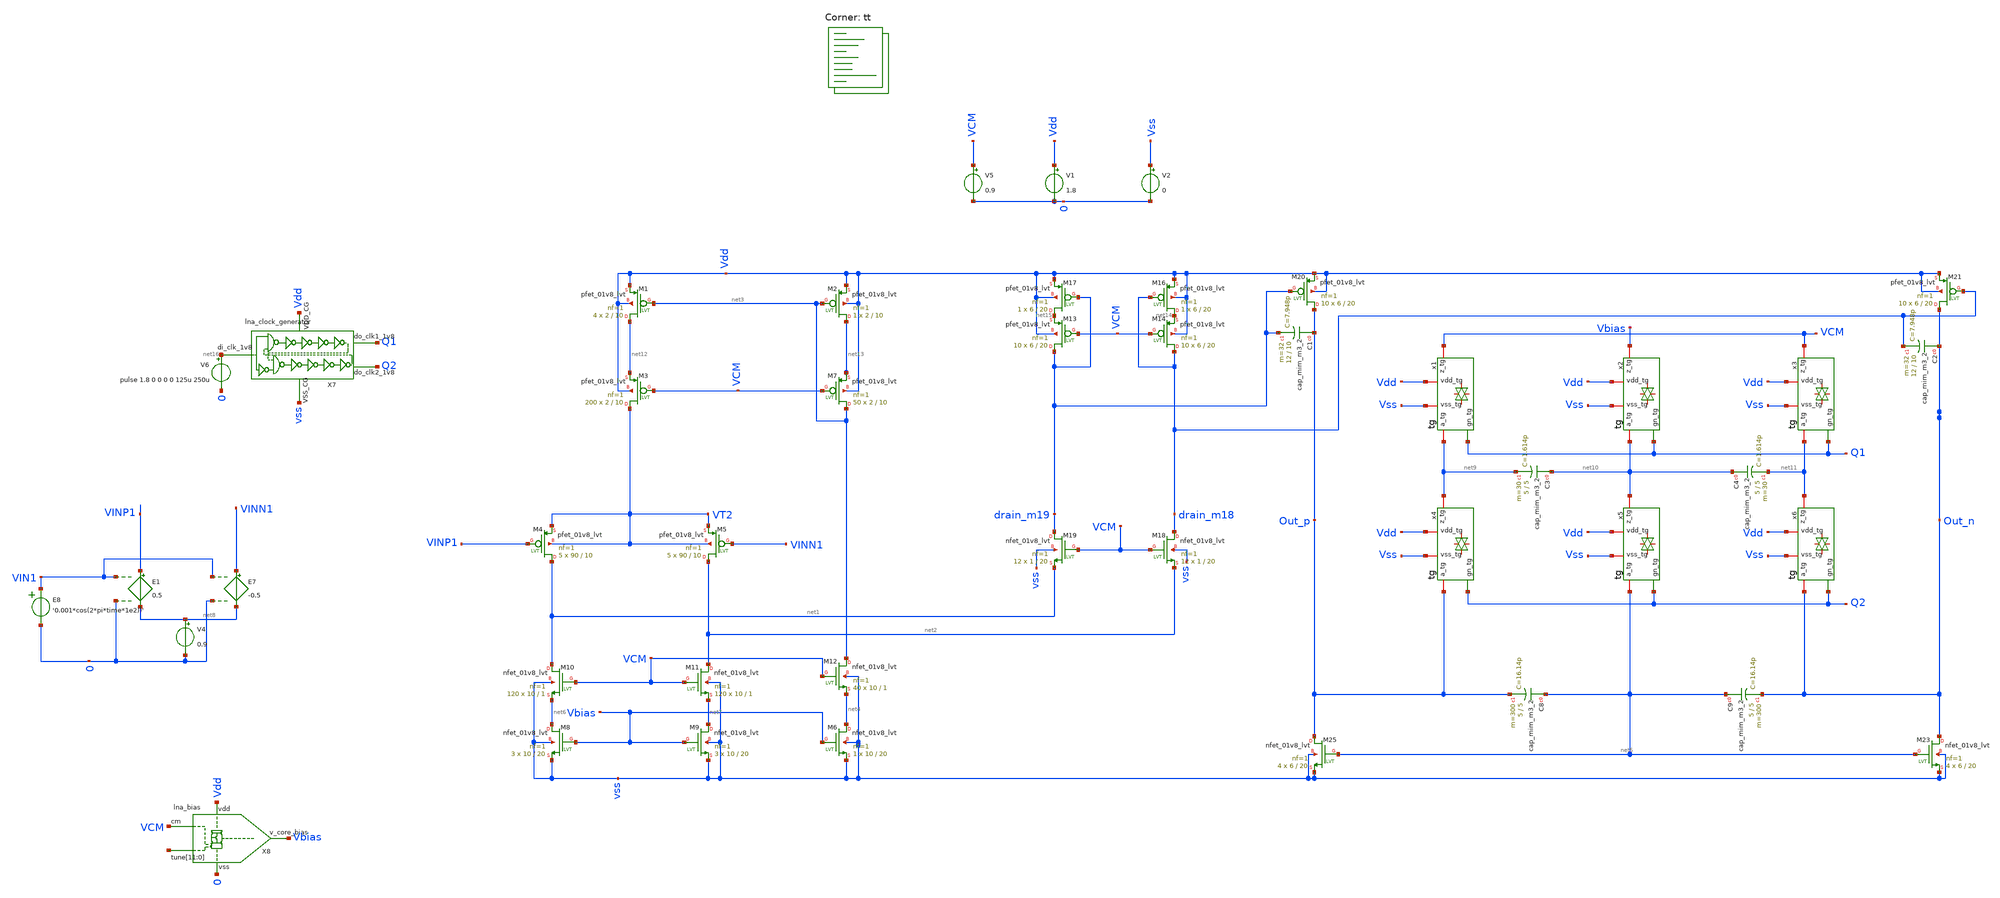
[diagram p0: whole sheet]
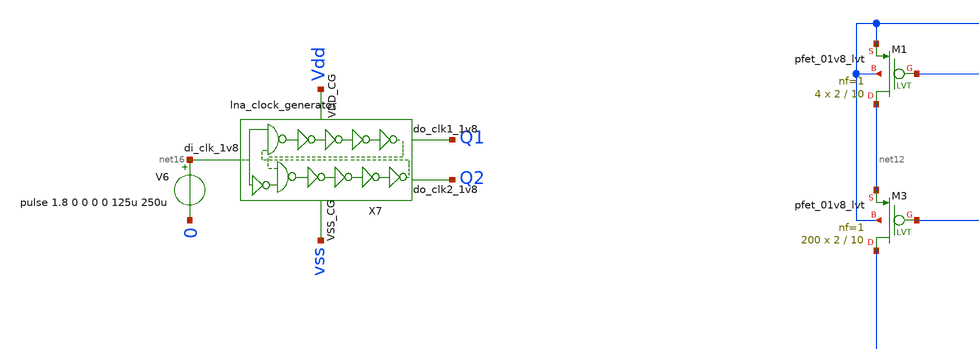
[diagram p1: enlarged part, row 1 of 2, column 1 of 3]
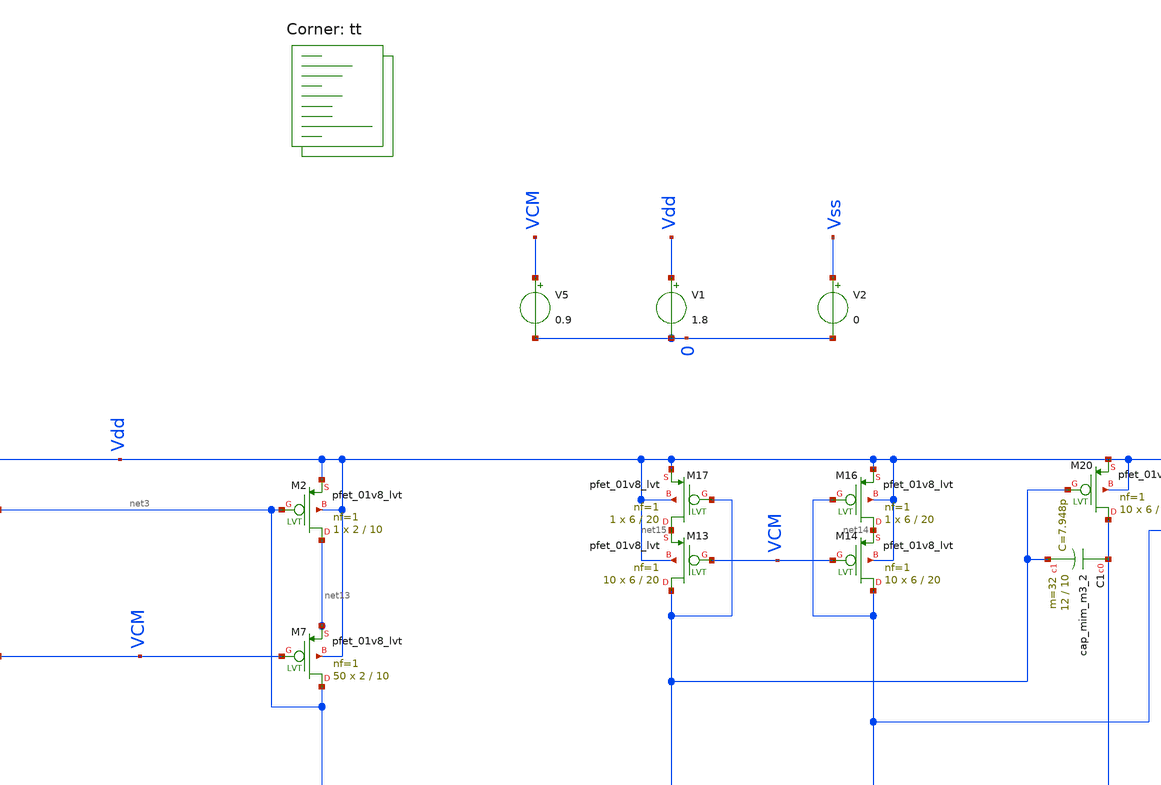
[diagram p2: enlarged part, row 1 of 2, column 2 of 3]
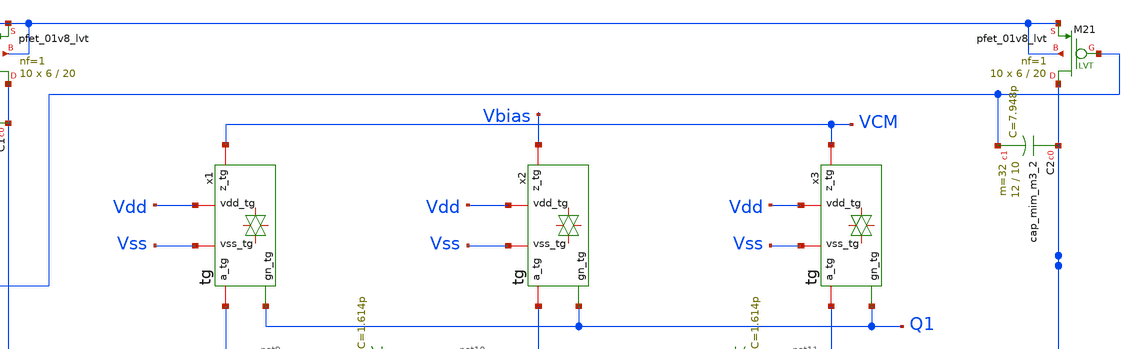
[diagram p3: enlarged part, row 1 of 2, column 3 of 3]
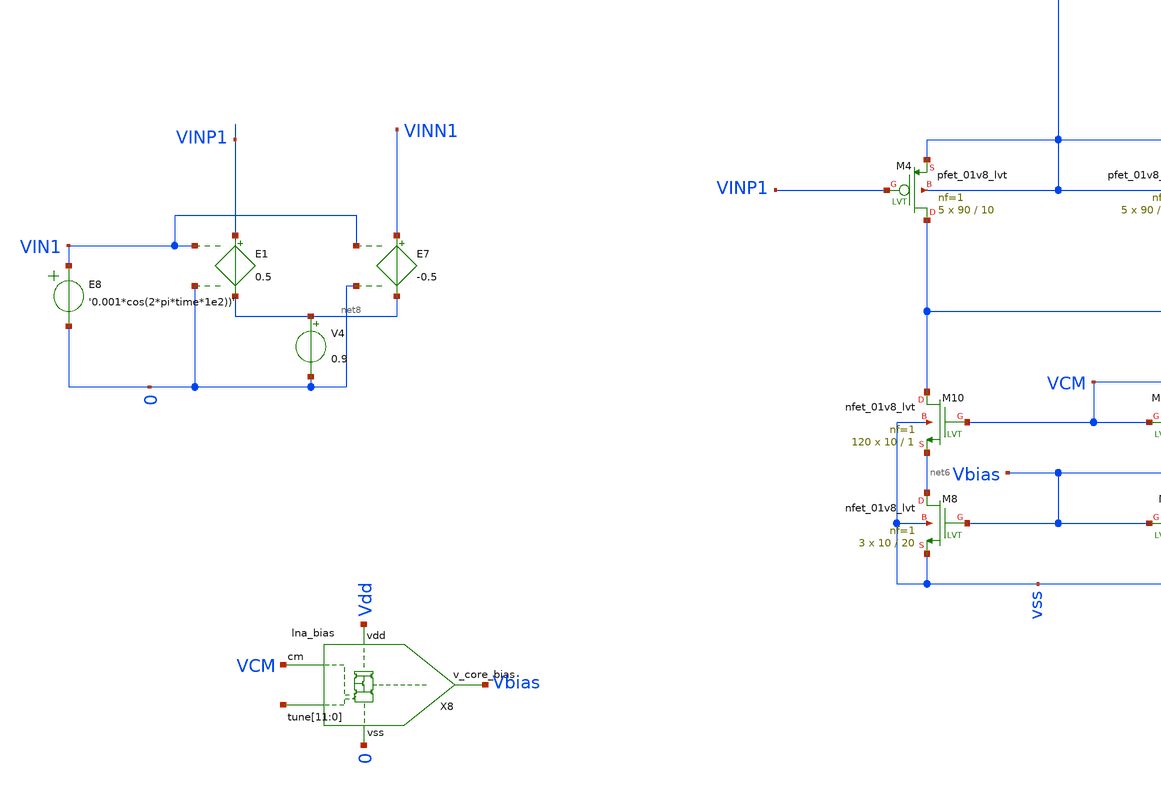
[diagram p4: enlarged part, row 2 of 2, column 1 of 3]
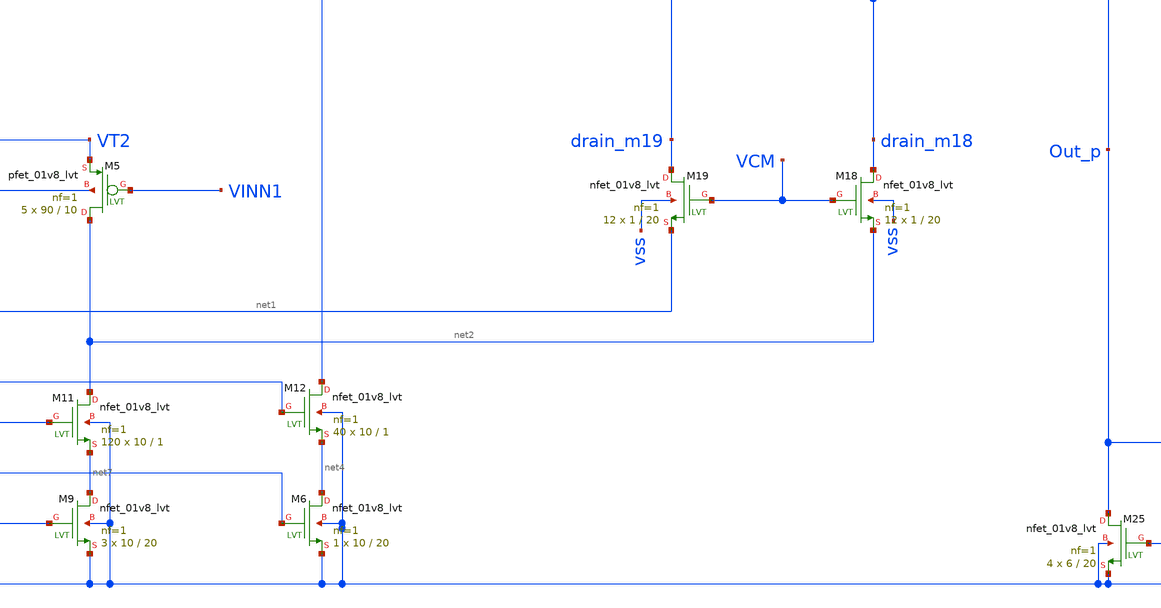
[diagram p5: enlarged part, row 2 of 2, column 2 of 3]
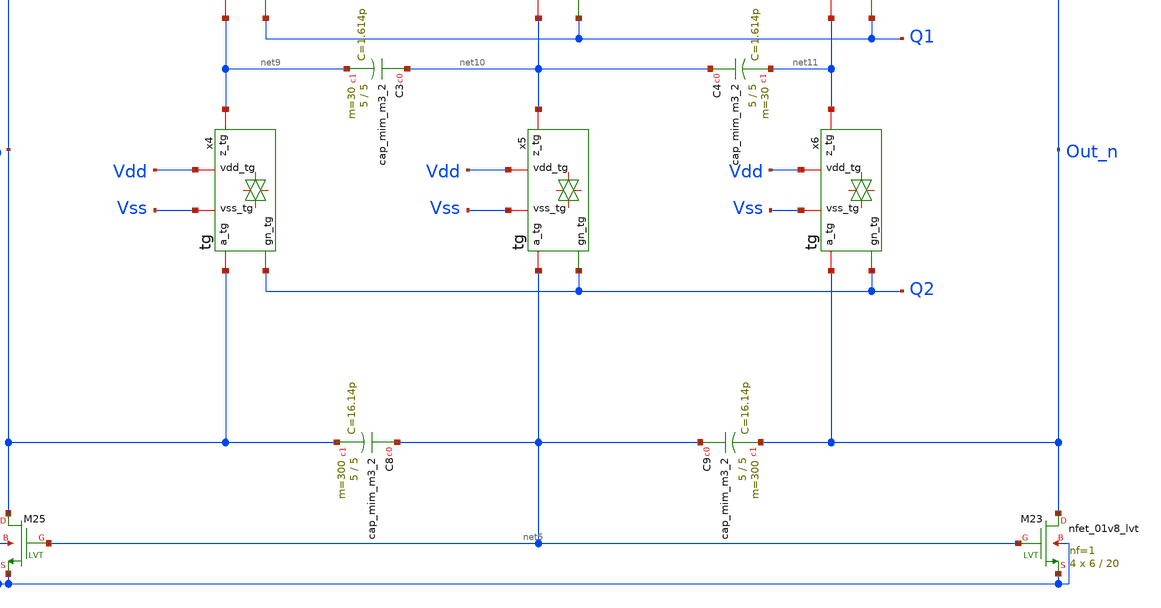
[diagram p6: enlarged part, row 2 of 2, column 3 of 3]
** sch_path: OL_transient.sch
**.subckt OL_transient
XM4 net1 VINP1 VT2 VT2 sky130_fd_pr__pfet_01v8_lvt L=10 W=90 nf=1 ad='int((nf+1)/2) * W/nf * 0.29' as='int((nf+2)/2) * W/nf * 0.29'
+ pd='2*int((nf+1)/2) * (W/nf + 0.29)' ps='2*int((nf+2)/2) * (W/nf + 0.29)' nrd='0.29 / W' nrs='0.29 / W'
+ sa=0 sb=0 sd=0 mult=5 m=5
XM5 net2 VINN1 VT2 VT2 sky130_fd_pr__pfet_01v8_lvt L=10 W=90 nf=1 ad='int((nf+1)/2) * W/nf * 0.29' as='int((nf+2)/2) * W/nf * 0.29'
+ pd='2*int((nf+1)/2) * (W/nf + 0.29)' ps='2*int((nf+2)/2) * (W/nf + 0.29)' nrd='0.29 / W' nrs='0.29 / W'
+ sa=0 sb=0 sd=0 mult=5 m=5
XM8 net6 Vbias vss vss sky130_fd_pr__nfet_01v8_lvt L=20 W=10 nf=1 ad='int((nf+1)/2) * W/nf * 0.29' as='int((nf+2)/2) * W/nf * 0.29'
+ pd='2*int((nf+1)/2) * (W/nf + 0.29)' ps='2*int((nf+2)/2) * (W/nf + 0.29)' nrd='0.29 / W' nrs='0.29 / W'
+ sa=0 sb=0 sd=0 mult=3 m=3
XM9 net7 Vbias vss vss sky130_fd_pr__nfet_01v8_lvt L=20 W=10 nf=1 ad='int((nf+1)/2) * W/nf * 0.29' as='int((nf+2)/2) * W/nf * 0.29'
+ pd='2*int((nf+1)/2) * (W/nf + 0.29)' ps='2*int((nf+2)/2) * (W/nf + 0.29)' nrd='0.29 / W' nrs='0.29 / W'
+ sa=0 sb=0 sd=0 mult=3 m=3
XM16 net14 drain_m18 Vdd Vdd sky130_fd_pr__pfet_01v8_lvt L=20 W=6 nf=1 ad='int((nf+1)/2) * W/nf * 0.29'
+ as='int((nf+2)/2) * W/nf * 0.29' pd='2*int((nf+1)/2) * (W/nf + 0.29)' ps='2*int((nf+2)/2) * (W/nf + 0.29)'
+ nrd='0.29 / W' nrs='0.29 / W' sa=0 sb=0 sd=0 mult=1 m=1
XM17 net15 drain_m19 Vdd Vdd sky130_fd_pr__pfet_01v8_lvt L=20 W=6 nf=1 ad='int((nf+1)/2) * W/nf * 0.29'
+ as='int((nf+2)/2) * W/nf * 0.29' pd='2*int((nf+1)/2) * (W/nf + 0.29)' ps='2*int((nf+2)/2) * (W/nf + 0.29)'
+ nrd='0.29 / W' nrs='0.29 / W' sa=0 sb=0 sd=0 mult=1 m=1
XM18 drain_m18 VCM net2 vss sky130_fd_pr__nfet_01v8_lvt L=20 W=1 nf=1 ad='int((nf+1)/2) * W/nf * 0.29'
+ as='int((nf+2)/2) * W/nf * 0.29' pd='2*int((nf+1)/2) * (W/nf + 0.29)' ps='2*int((nf+2)/2) * (W/nf + 0.29)'
+ nrd='0.29 / W' nrs='0.29 / W' sa=0 sb=0 sd=0 mult=12 m=12
XM19 drain_m19 VCM net1 vss sky130_fd_pr__nfet_01v8_lvt L=20 W=1 nf=1 ad='int((nf+1)/2) * W/nf * 0.29'
+ as='int((nf+2)/2) * W/nf * 0.29' pd='2*int((nf+1)/2) * (W/nf + 0.29)' ps='2*int((nf+2)/2) * (W/nf + 0.29)'
+ nrd='0.29 / W' nrs='0.29 / W' sa=0 sb=0 sd=0 mult=12 m=12
XM20 Out_p drain_m19 Vdd Vdd sky130_fd_pr__pfet_01v8_lvt L=20 W=6 nf=1 ad='int((nf+1)/2) * W/nf * 0.29'
+ as='int((nf+2)/2) * W/nf * 0.29' pd='2*int((nf+1)/2) * (W/nf + 0.29)' ps='2*int((nf+2)/2) * (W/nf + 0.29)'
+ nrd='0.29 / W' nrs='0.29 / W' sa=0 sb=0 sd=0 mult=10 m=10
XM21 Out_n drain_m18 Vdd Vdd sky130_fd_pr__pfet_01v8_lvt L=20 W=6 nf=1 ad='int((nf+1)/2) * W/nf * 0.29'
+ as='int((nf+2)/2) * W/nf * 0.29' pd='2*int((nf+1)/2) * (W/nf + 0.29)' ps='2*int((nf+2)/2) * (W/nf + 0.29)'
+ nrd='0.29 / W' nrs='0.29 / W' sa=0 sb=0 sd=0 mult=10 m=10
XM23 Out_n net5 vss vss sky130_fd_pr__nfet_01v8_lvt L=20 W=6 nf=1 ad='int((nf+1)/2) * W/nf * 0.29' as='int((nf+2)/2) * W/nf * 0.29'
+ pd='2*int((nf+1)/2) * (W/nf + 0.29)' ps='2*int((nf+2)/2) * (W/nf + 0.29)' nrd='0.29 / W' nrs='0.29 / W'
+ sa=0 sb=0 sd=0 mult=4 m=4
XM25 Out_p net5 vss vss sky130_fd_pr__nfet_01v8_lvt L=20 W=6 nf=1 ad='int((nf+1)/2) * W/nf * 0.29' as='int((nf+2)/2) * W/nf * 0.29'
+ pd='2*int((nf+1)/2) * (W/nf + 0.29)' ps='2*int((nf+2)/2) * (W/nf + 0.29)' nrd='0.29 / W' nrs='0.29 / W'
+ sa=0 sb=0 sd=0 mult=4 m=4
V1 Vdd 0 1.8
V2 Vss 0 0
V5 VCM 0 0.9
XM1 net12 net3 Vdd Vdd sky130_fd_pr__pfet_01v8_lvt L=10 W=2 nf=1 ad='int((nf+1)/2) * W/nf * 0.29' as='int((nf+2)/2) * W/nf * 0.29'
+ pd='2*int((nf+1)/2) * (W/nf + 0.29)' ps='2*int((nf+2)/2) * (W/nf + 0.29)' nrd='0.29 / W' nrs='0.29 / W'
+ sa=0 sb=0 sd=0 mult=4 m=4
XM2 net13 net3 Vdd Vdd sky130_fd_pr__pfet_01v8_lvt L=10 W=2 nf=1 ad='int((nf+1)/2) * W/nf * 0.29' as='int((nf+2)/2) * W/nf * 0.29'
+ pd='2*int((nf+1)/2) * (W/nf + 0.29)' ps='2*int((nf+2)/2) * (W/nf + 0.29)' nrd='0.29 / W' nrs='0.29 / W'
+ sa=0 sb=0 sd=0 mult=1 m=1
XM6 net4 Vbias vss vss sky130_fd_pr__nfet_01v8_lvt L=20 W=10 nf=1 ad='int((nf+1)/2) * W/nf * 0.29' as='int((nf+2)/2) * W/nf * 0.29'
+ pd='2*int((nf+1)/2) * (W/nf + 0.29)' ps='2*int((nf+2)/2) * (W/nf + 0.29)' nrd='0.29 / W' nrs='0.29 / W'
+ sa=0 sb=0 sd=0 mult=1 m=1
E1 VINP1 net8 VIN1 0 0.5
E7 VINN1 net8 VIN1 0 -0.5
V4 net8 0 0.9
E8 VIN1 0 VOL=' '0.001*cos(2*pi*time*1e2))' '
XC3 net10 net9 sky130_fd_pr__cap_mim_m3_2 W=5 L=5 MF=30 m=30
XC4 net10 net11 sky130_fd_pr__cap_mim_m3_2 W=5 L=5 MF=30 m=30
XC8 net5 Out_p sky130_fd_pr__cap_mim_m3_2 W=5 L=5 MF=300 m=300
XC9 net5 Out_n sky130_fd_pr__cap_mim_m3_2 W=5 L=5 MF=300 m=300
x1 Vdd net9 VCM Vss Q1 tg
x2 Vdd net10 Vbias Vss Q1 tg
x3 Vdd net11 VCM Vss Q1 tg
x4 Vdd Out_p net9 Vss Q2 tg
x5 Vdd net5 net10 Vss Q2 tg
x6 Vdd Out_n net11 Vss Q2 tg
V6 net16 0 pulse 1.8 0 0 0 0 125u 250u
X7 net16 vss Q1 Q2 Vdd lna_clock_generator
X8 VCM Vdd 0 Vbias net17[11] net17[10] net17[9] net17[8] net17[7] net17[6] net17[5] net17[4]
+ net17[3] net17[2] net17[1] net17[0] lna_bias
XC1 Out_p drain_m19 sky130_fd_pr__cap_mim_m3_2 W=12 L=10 MF=32 m=32
XC2 Out_n drain_m18 sky130_fd_pr__cap_mim_m3_2 W=12 L=10 MF=32 m=32
XM3 VT2 VCM net12 Vdd sky130_fd_pr__pfet_01v8_lvt L=10 W=2 nf=1 ad='int((nf+1)/2) * W/nf * 0.29' as='int((nf+2)/2) * W/nf * 0.29'
+ pd='2*int((nf+1)/2) * (W/nf + 0.29)' ps='2*int((nf+2)/2) * (W/nf + 0.29)' nrd='0.29 / W' nrs='0.29 / W'
+ sa=0 sb=0 sd=0 mult=200 m=200
XM7 net3 VCM net13 Vdd sky130_fd_pr__pfet_01v8_lvt L=10 W=2 nf=1 ad='int((nf+1)/2) * W/nf * 0.29' as='int((nf+2)/2) * W/nf * 0.29'
+ pd='2*int((nf+1)/2) * (W/nf + 0.29)' ps='2*int((nf+2)/2) * (W/nf + 0.29)' nrd='0.29 / W' nrs='0.29 / W'
+ sa=0 sb=0 sd=0 mult=50 m=50
XM10 net1 VCM net6 vss sky130_fd_pr__nfet_01v8_lvt L=1 W=10 nf=1 ad='int((nf+1)/2) * W/nf * 0.29' as='int((nf+2)/2) * W/nf * 0.29'
+ pd='2*int((nf+1)/2) * (W/nf + 0.29)' ps='2*int((nf+2)/2) * (W/nf + 0.29)' nrd='0.29 / W' nrs='0.29 / W'
+ sa=0 sb=0 sd=0 mult=120 m=120
XM11 net2 VCM net7 vss sky130_fd_pr__nfet_01v8_lvt L=1 W=10 nf=1 ad='int((nf+1)/2) * W/nf * 0.29' as='int((nf+2)/2) * W/nf * 0.29'
+ pd='2*int((nf+1)/2) * (W/nf + 0.29)' ps='2*int((nf+2)/2) * (W/nf + 0.29)' nrd='0.29 / W' nrs='0.29 / W'
+ sa=0 sb=0 sd=0 mult=120 m=120
XM12 net3 VCM net4 vss sky130_fd_pr__nfet_01v8_lvt L=1 W=10 nf=1 ad='int((nf+1)/2) * W/nf * 0.29' as='int((nf+2)/2) * W/nf * 0.29'
+ pd='2*int((nf+1)/2) * (W/nf + 0.29)' ps='2*int((nf+2)/2) * (W/nf + 0.29)' nrd='0.29 / W' nrs='0.29 / W'
+ sa=0 sb=0 sd=0 mult=40 m=40
XM13 drain_m19 VCM net15 Vdd sky130_fd_pr__pfet_01v8_lvt L=20 W=6 nf=1 ad='int((nf+1)/2) * W/nf * 0.29'
+ as='int((nf+2)/2) * W/nf * 0.29' pd='2*int((nf+1)/2) * (W/nf + 0.29)' ps='2*int((nf+2)/2) * (W/nf + 0.29)'
+ nrd='0.29 / W' nrs='0.29 / W' sa=0 sb=0 sd=0 mult=10 m=10
XM14 drain_m18 VCM net14 Vdd sky130_fd_pr__pfet_01v8_lvt L=20 W=6 nf=1 ad='int((nf+1)/2) * W/nf * 0.29'
+ as='int((nf+2)/2) * W/nf * 0.29' pd='2*int((nf+1)/2) * (W/nf + 0.29)' ps='2*int((nf+2)/2) * (W/nf + 0.29)'
+ nrd='0.29 / W' nrs='0.29 / W' sa=0 sb=0 sd=0 mult=10 m=10
**** begin user architecture code
.lib $::SKYWATER_MODELS/sky130.lib.spice tt


.options savecurrents
*ic v(VM5)=0.9 v(VM6)=0.9
.control


save all

save @m.xm11.msky130_fd_pr__pfet_01v8_lvt[id]
save @m.xm11.msky130_fd_pr__pfet_01v8_lvt[vgs]


*nmos
save @m.xm3.msky130_fd_pr__nfet_01v8_lvt[vgs]
save @m.xm3.msky130_fd_pr__nfet_01v8_lvt[vth]
save @m.xm3.msky130_fd_pr__nfet_01v8_lvt[vds]

save @m.xm6.msky130_fd_pr__nfet_01v8_lvt[vgs]
save @m.xm6.msky130_fd_pr__nfet_01v8_lvt[vth]
save @m.xm6.msky130_fd_pr__nfet_01v8_lvt[vds]

save @m.xm8.msky130_fd_pr__nfet_01v8_lvt[vgs]
save @m.xm8.msky130_fd_pr__nfet_01v8_lvt[vth]
save @m.xm8.msky130_fd_pr__nfet_01v8_lvt[vds]

save @m.xm9.msky130_fd_pr__nfet_01v8_lvt[vgs]
save @m.xm9.msky130_fd_pr__nfet_01v8_lvt[vth]
save @m.xm9.msky130_fd_pr__nfet_01v8_lvt[vds]

save @m.xm10.msky130_fd_pr__nfet_01v8_lvt[vgs]
save @m.xm10.msky130_fd_pr__nfet_01v8_lvt[vth]
save @m.xm10.msky130_fd_pr__nfet_01v8_lvt[vds]

save @m.xm11.msky130_fd_pr__nfet_01v8_lvt[vgs]
save @m.xm11.msky130_fd_pr__nfet_01v8_lvt[vth]
save @m.xm11.msky130_fd_pr__nfet_01v8_lvt[vds]

save @m.xm12.msky130_fd_pr__nfet_01v8_lvt[vgs]
save @m.xm12.msky130_fd_pr__nfet_01v8_lvt[vth]
save @m.xm12.msky130_fd_pr__nfet_01v8_lvt[vds]

save @m.xm18.msky130_fd_pr__nfet_01v8_lvt[vgs]
save @m.xm18.msky130_fd_pr__nfet_01v8_lvt[vth]
save @m.xm18.msky130_fd_pr__nfet_01v8_lvt[vds]

save @m.xm19.msky130_fd_pr__nfet_01v8_lvt[vgs]
save @m.xm19.msky130_fd_pr__nfet_01v8_lvt[vth]
save @m.xm19.msky130_fd_pr__nfet_01v8_lvt[vds]

save @m.xm25.msky130_fd_pr__nfet_01v8_lvt[vgs]
save @m.xm25.msky130_fd_pr__nfet_01v8_lvt[vth]
save @m.xm25.msky130_fd_pr__nfet_01v8_lvt[vds]

*pmos

save @m.xm1.msky130_fd_pr__pfet_01v8_lvt[vgs]
save @m.xm1.msky130_fd_pr__pfet_01v8_lvt[vth]
save @m.xm1.msky130_fd_pr__pfet_01v8_lvt[vds]


save @m.xm2.msky130_fd_pr__pfet_01v8_lvt[vgs]
save @m.xm2.msky130_fd_pr__pfet_01v8_lvt[vth]
save @m.xm2.msky130_fd_pr__pfet_01v8_lvt[vds]

save @m.xm7.msky130_fd_pr__pfet_01v8_lvt[vgs]
save @m.xm7.msky130_fd_pr__pfet_01v8_lvt[vth]
save @m.xm7.msky130_fd_pr__pfet_01v8_lvt[vds]


save @m.xm10.msky130_fd_pr__pfet_01v8_lvt[vgs]
save @m.xm10.msky130_fd_pr__pfet_01v8_lvt[vth]
save @m.xm10.msky130_fd_pr__pfet_01v8_lvt[vds]

save @m.xm13.msky130_fd_pr__pfet_01v8_lvt[vgs]
save @m.xm13.msky130_fd_pr__pfet_01v8_lvt[vth]
save @m.xm13.msky130_fd_pr__pfet_01v8_lvt[vds]

save @m.xm14.msky130_fd_pr__pfet_01v8_lvt[vgs]
save @m.xm14.msky130_fd_pr__pfet_01v8_lvt[vth]
save @m.xm14.msky130_fd_pr__pfet_01v8_lvt[vds]

save @m.xm4.msky130_fd_pr__pfet_01v8_lvt[vgs]
save @m.xm4.msky130_fd_pr__pfet_01v8_lvt[vth]
save @m.xm4.msky130_fd_pr__pfet_01v8_lvt[vds]

save @m.xm5.msky130_fd_pr__pfet_01v8_lvt[vgs]
save @m.xm5.msky130_fd_pr__pfet_01v8_lvt[vth]
save @m.xm5.msky130_fd_pr__pfet_01v8_lvt[vds]

save @m.xm16.msky130_fd_pr__pfet_01v8_lvt[vgs]
save @m.xm16.msky130_fd_pr__pfet_01v8_lvt[vth]
save @m.xm16.msky130_fd_pr__pfet_01v8_lvt[vds]

save @m.xm17.msky130_fd_pr__pfet_01v8_lvt[vgs]
save @m.xm17.msky130_fd_pr__pfet_01v8_lvt[vth]
save @m.xm17.msky130_fd_pr__pfet_01v8_lvt[vds]

save @m.xm3.msky130_fd_pr__pfet_01v8_lvt[vgs]
save @m.xm3.msky130_fd_pr__pfet_01v8_lvt[vth]
save @m.xm3.msky130_fd_pr__pfet_01v8_lvt[vds]

save @m.xm20.msky130_fd_pr__pfet_01v8_lvt[vgs]
save @m.xm20.msky130_fd_pr__pfet_01v8_lvt[vth]
save @m.xm20.msky130_fd_pr__pfet_01v8_lvt[vds]

save @m.xm2.msky130_fd_pr__pfet_01v8_lvt[vgs]
save @m.xm2.msky130_fd_pr__pfet_01v8_lvt[vth]
save @m.xm2.msky130_fd_pr__pfet_01v8_lvt[vds]

save @m.xm21.msky130_fd_pr__pfet_01v8_lvt[vgs]
save @m.xm21.msky130_fd_pr__pfet_01v8_lvt[vth]
save @m.xm21.msky130_fd_pr__pfet_01v8_lvt[vds]

save @m.xm7.msky130_fd_pr__nfet_01v8_lvt[vth]

save @m.xm1.msky130_fd_pr__pfet_01v8[vgs]

save @m.xm1.msky130_fd_pr__nfet_01v8_lvt[gm]


save @m.xm1.msky130_fd_pr__nfet_01v8_lvt[gds]
save @m.xm2.msky130_fd_pr__pfet_01v8_lvt[gm]

save @m.xm23.msky130_fd_pr__nfet_01v8[cgs]
save @m.xm4.msky130_fd_pr__pfet_01v8[cgs]
save @m.xm2.msky130_fd_pr__pfet_01v8_lvt[cgs]



save @m.xm2.msky130_fd_pr__pfet_01v8_lvt[gds]


op
*remzerovec
write OL_transient.raw
*set appendwrite

*dc V1 0 1.8 0.01
*plot @m.xm1.msky130_fd_pr__nfet_01v8_lvt[id] @m.xm2.msky130_fd_pr__pfet_01v8_lvt[id]
*remzerovec
*write OL_transient.raw

.endc
.control
let vth=@M.XM25.msky130_fd_pr__nfet_01v8_lvt[vgs]


noise V(Out_p,Out_n) V6 dec 100 0.1 128
print inoise_total onoise_total
setplot noise1
plot inoise_spectrum




tran 10u 100m
save all
plot v(Out_p)
plot v(Out_p)-v(Out_n)
plot v(@m.xm25.msky130_fd_pr__nfet_01v8_lvt[vth]) v(@m.xm25.msky130_fd_pr__nfet_01v8_lvt[vgs])
plot
+ v(@m.xm25.msky130_fd_pr__nfet_01v8_lvt[vds])-v(@m.xm25.msky130_fd_pr__nfet_01v8_lvt[vgs])+v(@m.xm25.msky130_fd_pr__nfet_01v8_lvt[vth])

.endc






.include $::SKYWATER_STDCELLS/sky130_fd_sc_hd.spice

**** end user architecture code
**.ends
.end
